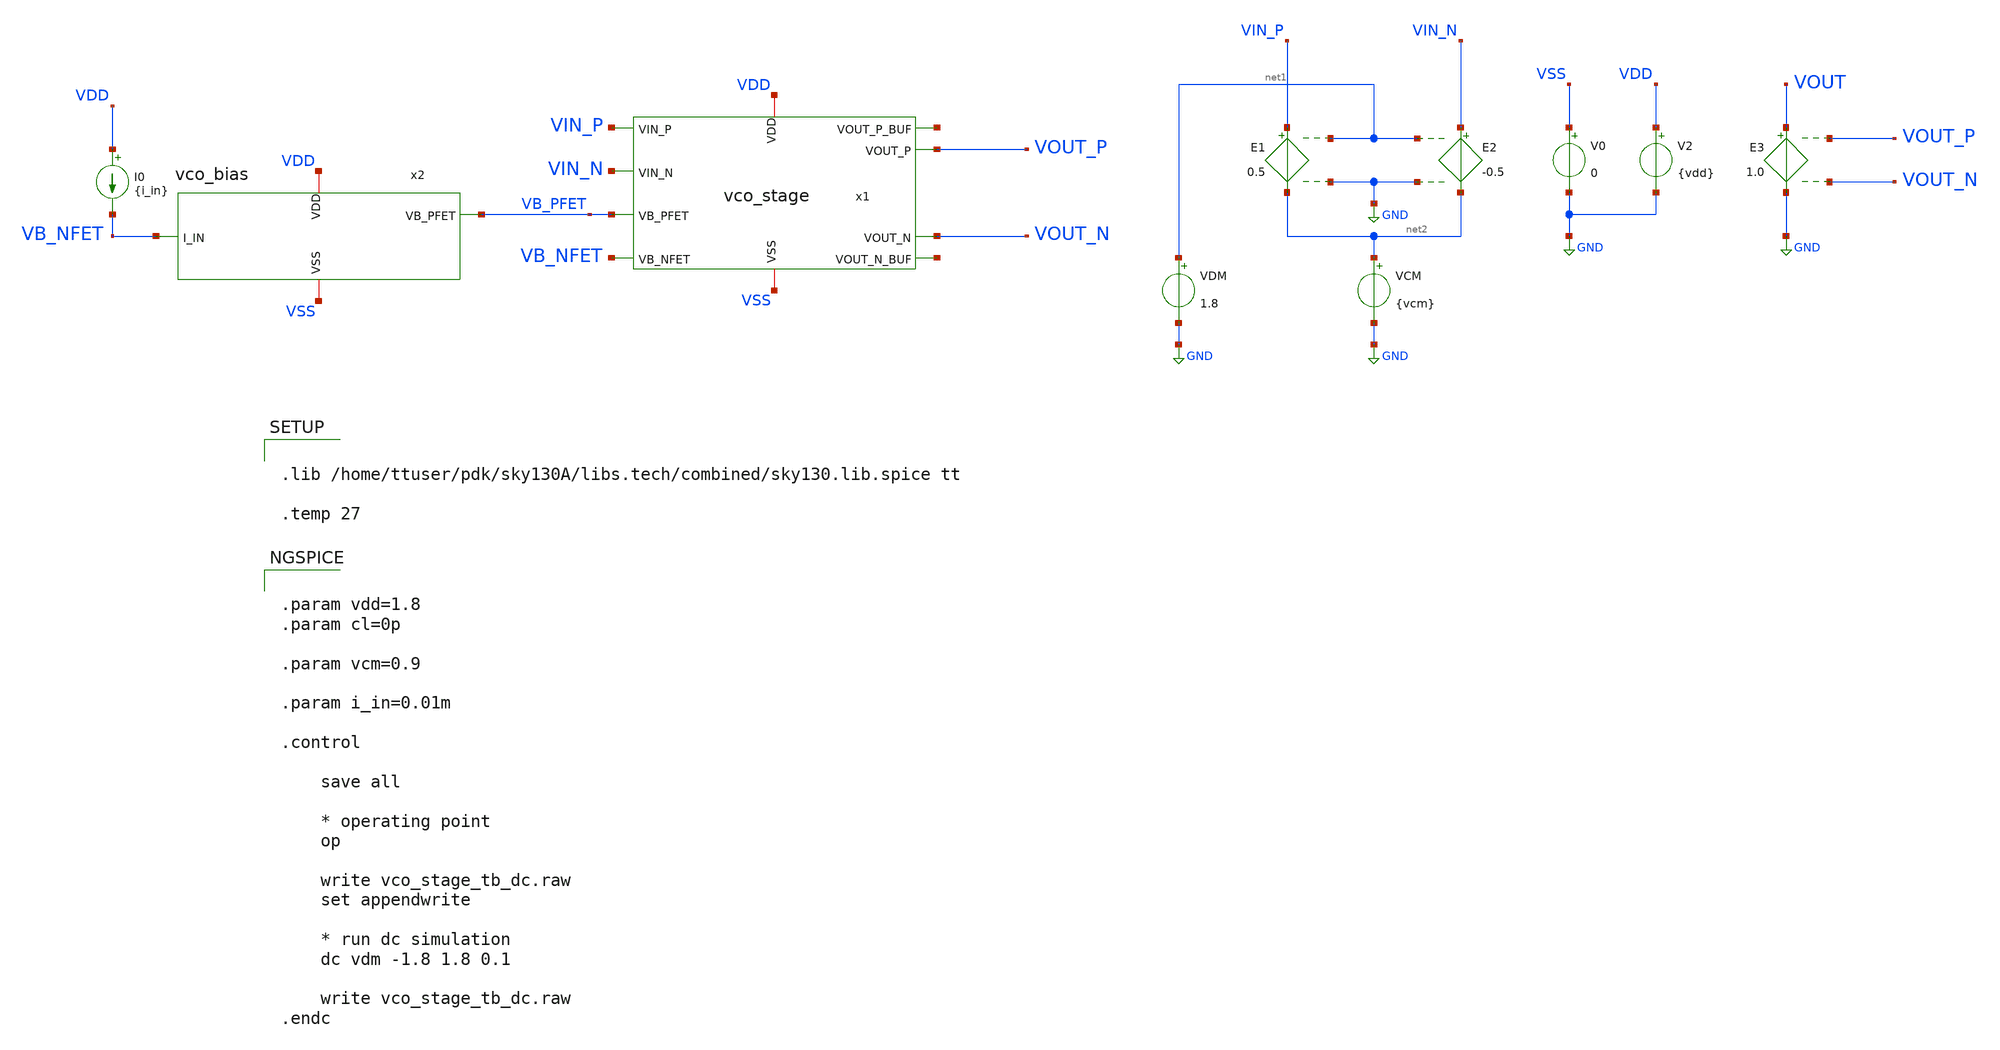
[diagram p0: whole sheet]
** sch_path: xschem/vco_stage_tb_dc.sch
**.subckt vco_stage_tb_dc
E1 VIN_P net2 net1 GND 0.5
E2 VIN_N net2 net1 GND -0.5
VDM net1 GND 1.8
VCM net2 GND {vcm}
V0 VSS GND 0
V2 VDD GND {vdd}
E3 VOUT GND VOUT_P VOUT_N 1.0
x1 VDD VSS VIN_P VIN_N VB_PFET VB_NFET VOUT_P VOUT_N net3 net4 vco_stage
x2 VDD VSS VB_NFET VB_PFET vco_bias
I0 VDD VB_NFET {i_in}
**** begin user architecture code


.param vdd=1.8
.param cl=0p

.param vcm=0.9

.param i_in=0.01m

.control

    save all

    * operating point
    op

    write vco_stage_tb_dc.raw
    set appendwrite

    * run dc simulation
    dc vdm -1.8 1.8 0.1

    write vco_stage_tb_dc.raw
.endc




.lib /home/ttuser/pdk/sky130A/libs.tech/combined/sky130.lib.spice tt

.temp 27


**** end user architecture code
**.ends

* expanding   symbol:  vco_stage.sym # of pins=10
** sym_path: xschem/vco_stage.sym
** sch_path: xschem/vco_stage.sch
.subckt vco_stage VDD VSS VIN_P VIN_N VB_PFET VB_NFET VOUT_P VOUT_N VOUT_P_BUF VOUT_N_BUF
*.iopin VDD
*.iopin VSS
*.ipin VIN_P
*.ipin VIN_N
*.ipin VB_PFET
*.ipin VB_NFET
*.opin VOUT_P
*.opin VOUT_N
*.opin VOUT_P_BUF
*.opin VOUT_N_BUF
x1 VDD VSS VIN_P VB_PFET VOUT_N VOUT_P VDRAIN_M5 VOUT_P_BUF vco_stage_half
x2 VDD VSS VIN_N VB_PFET VOUT_P VOUT_N VDRAIN_M5 VOUT_N_BUF vco_stage_half
XM5 VDRAIN_M5 VB_NFET VSS VSS sky130_fd_pr__nfet_01v8 L=2 W=4 nf=2 ad='int((nf+1)/2) * W/nf * 0.29' as='int((nf+2)/2) * W/nf * 0.29'
+ pd='2*int((nf+1)/2) * (W/nf + 0.29)' ps='2*int((nf+2)/2) * (W/nf + 0.29)' nrd='0.29 / W' nrs='0.29 / W'
+ sa=0 sb=0 sd=0 mult=1 m=1
.ends


* expanding   symbol:  vco_bias.sym # of pins=4
** sym_path: xschem/vco_bias.sym
** sch_path: xschem/vco_bias.sch
.subckt vco_bias VDD VSS I_IN VB_PFET
*.iopin VDD
*.iopin VSS
*.ipin I_IN
*.opin VB_PFET
XM1 I_IN I_IN VSS VSS sky130_fd_pr__nfet_01v8 L=2 W=4 nf=2 ad='int((nf+1)/2) * W/nf * 0.29' as='int((nf+2)/2) * W/nf * 0.29'
+ pd='2*int((nf+1)/2) * (W/nf + 0.29)' ps='2*int((nf+2)/2) * (W/nf + 0.29)' nrd='0.29 / W' nrs='0.29 / W'
+ sa=0 sb=0 sd=0 mult=1 m=1
XM2 VB_PFET I_IN VSS VSS sky130_fd_pr__nfet_01v8 L=2 W=4 nf=2 ad='int((nf+1)/2) * W/nf * 0.29' as='int((nf+2)/2) * W/nf * 0.29'
+ pd='2*int((nf+1)/2) * (W/nf + 0.29)' ps='2*int((nf+2)/2) * (W/nf + 0.29)' nrd='0.29 / W' nrs='0.29 / W'
+ sa=0 sb=0 sd=0 mult=1 m=1
XM3 VB_PFET VB_PFET VDD VDD sky130_fd_pr__pfet_01v8 L=0.25 W=4 nf=1 ad='int((nf+1)/2) * W/nf * 0.29'
+ as='int((nf+2)/2) * W/nf * 0.29' pd='2*int((nf+1)/2) * (W/nf + 0.29)' ps='2*int((nf+2)/2) * (W/nf + 0.29)'
+ nrd='0.29 / W' nrs='0.29 / W' sa=0 sb=0 sd=0 mult=1 m=1
.ends


* expanding   symbol:  vco_stage_half.sym # of pins=8
** sym_path: xschem/vco_stage_half.sym
** sch_path: xschem/vco_stage_half.sch
.subckt vco_stage_half VDD VSS VIN_DIFF VB_PFET VFB VOUT_DIFF VDRAIN_TAIL VOUT_DIFF_BUF
*.iopin VDD
*.iopin VSS
*.ipin VIN_DIFF
*.ipin VB_PFET
*.ipin VFB
*.opin VOUT_DIFF
*.opin VDRAIN_TAIL
*.opin VOUT_DIFF_BUF
XM7 VOUT_DIFF VFB VDD VDD sky130_fd_pr__pfet_01v8 L=2 W=4 nf=2 ad='int((nf+1)/2) * W/nf * 0.29' as='int((nf+2)/2) * W/nf * 0.29'
+ pd='2*int((nf+1)/2) * (W/nf + 0.29)' ps='2*int((nf+2)/2) * (W/nf + 0.29)' nrd='0.29 / W' nrs='0.29 / W'
+ sa=0 sb=0 sd=0 mult=1 m=1
XM3 VOUT_DIFF VB_PFET VDD VDD sky130_fd_pr__pfet_01v8 L=2 W=4 nf=2 ad='int((nf+1)/2) * W/nf * 0.29' as='int((nf+2)/2) * W/nf * 0.29'
+ pd='2*int((nf+1)/2) * (W/nf + 0.29)' ps='2*int((nf+2)/2) * (W/nf + 0.29)' nrd='0.29 / W' nrs='0.29 / W'
+ sa=0 sb=0 sd=0 mult=1 m=1
XM1 VOUT_DIFF VIN_DIFF VDRAIN_TAIL VSS sky130_fd_pr__nfet_01v8 L=2 W=4 nf=2 ad='int((nf+1)/2) * W/nf * 0.29'
+ as='int((nf+2)/2) * W/nf * 0.29' pd='2*int((nf+1)/2) * (W/nf + 0.29)' ps='2*int((nf+2)/2) * (W/nf + 0.29)'
+ nrd='0.29 / W' nrs='0.29 / W' sa=0 sb=0 sd=0 mult=1 m=1
x1 VDD VSS VOUT_DIFF VOUT_DIFF_BUF vco_buffer
XM8 VSS VOUT_DIFF VSS VSS sky130_fd_pr__nfet_01v8 L=11 W=11 nf=1 ad='int((nf+1)/2) * W/nf * 0.29' as='int((nf+2)/2) * W/nf * 0.29'
+ pd='2*int((nf+1)/2) * (W/nf + 0.29)' ps='2*int((nf+2)/2) * (W/nf + 0.29)' nrd='0.29 / W' nrs='0.29 / W'
+ sa=0 sb=0 sd=0 mult=1 m=1
.ends


* expanding   symbol:  vco_buffer.sym # of pins=4
** sym_path: xschem/vco_buffer.sym
** sch_path: xschem/vco_buffer.sch
.subckt vco_buffer VDD VSS VIN_BUF VOUT_BUF
*.iopin VDD
*.iopin VSS
*.ipin VIN_BUF
*.opin VOUT_BUF
x1 VDD VIN_BUF INT_BUF VSS vco_inverter
x2 VDD INT_BUF VOUT_BUF VSS vco_inverter
.ends


* expanding   symbol:  vco_inverter.sym # of pins=4
** sym_path: xschem/vco_inverter.sym
** sch_path: xschem/vco_inverter.sch
.subckt vco_inverter VDD VIN_INV VOUT_INV VSS
*.iopin VDD
*.iopin VSS
*.ipin VIN_INV
*.opin VOUT_INV
XM1 VOUT_INV VIN_INV VSS VSS sky130_fd_pr__nfet_01v8 L=0.15 W=1 nf=1 ad='int((nf+1)/2) * W/nf * 0.29'
+ as='int((nf+2)/2) * W/nf * 0.29' pd='2*int((nf+1)/2) * (W/nf + 0.29)' ps='2*int((nf+2)/2) * (W/nf + 0.29)'
+ nrd='0.29 / W' nrs='0.29 / W' sa=0 sb=0 sd=0 mult=1 m=1
XM2 VOUT_INV VIN_INV VDD VDD sky130_fd_pr__pfet_01v8 L=0.15 W=1 nf=1 ad='int((nf+1)/2) * W/nf * 0.29'
+ as='int((nf+2)/2) * W/nf * 0.29' pd='2*int((nf+1)/2) * (W/nf + 0.29)' ps='2*int((nf+2)/2) * (W/nf + 0.29)'
+ nrd='0.29 / W' nrs='0.29 / W' sa=0 sb=0 sd=0 mult=1 m=1
.ends

.GLOBAL GND
.end
